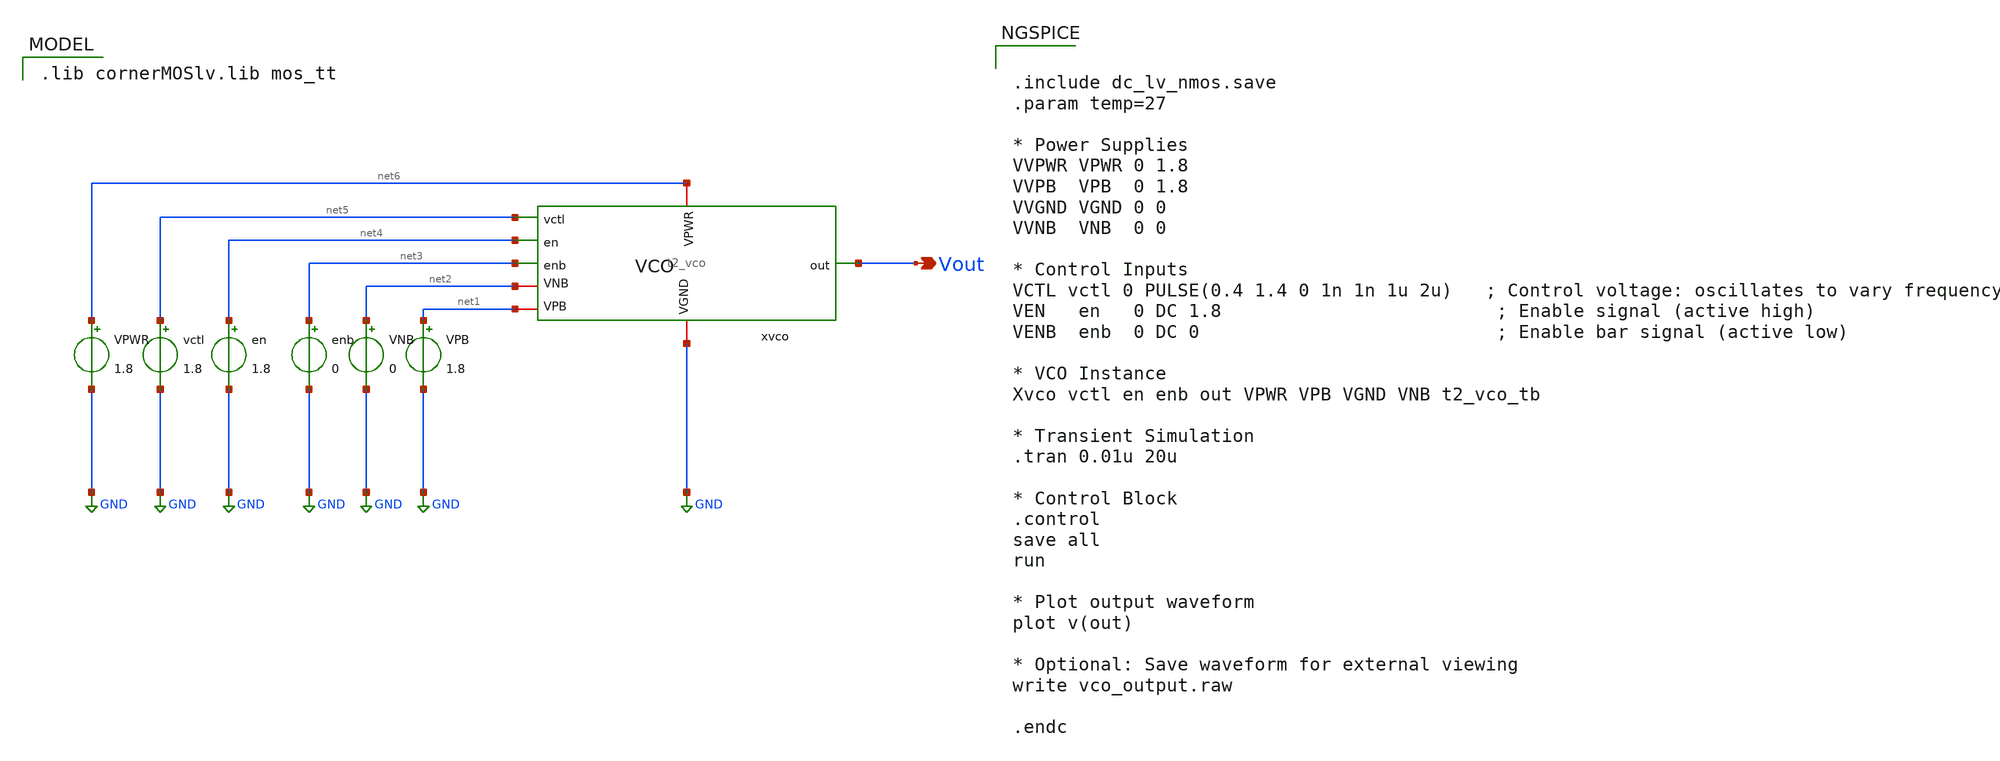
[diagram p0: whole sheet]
** sch_path: Team 2 Design/design_data/xschem/t2_vco_tb.sch
**.subckt t2_vco_tb Vout
*.opin Vout
x1 net6 net1 GND net2 Vout net5 net4 net3 t2_vco
VPWR net6 GND 1.8
vctl net5 GND 1.8
en net4 GND 1.8
enb net3 GND 0
VNB net2 GND 0
VPB net1 GND 1.8
**** begin user architecture code


.include dc_lv_nmos.save
.param temp=27

* Power Supplies
VVPWR VPWR 0 1.8
VVPB  VPB  0 1.8
VVGND VGND 0 0
VVNB  VNB  0 0

* Control Inputs
VCTL vctl 0 PULSE(0.4 1.4 0 1n 1n 1u 2u)   ; Control voltage: oscillates to vary frequency
VEN   en   0 DC 1.8                         ; Enable signal (active high)
VENB  enb  0 DC 0                           ; Enable bar signal (active low)

* VCO Instance
Xvco vctl en enb out VPWR VPB VGND VNB t2_vco_tb

* Transient Simulation
.tran 0.01u 20u

* Control Block
.control
save all
run

* Plot output waveform
plot v(out)

* Optional: Save waveform for external viewing
write vco_output.raw

.endc


 .lib cornerMOSlv.lib mos_tt

**** end user architecture code
**.ends
.GLOBAL GND
.end
